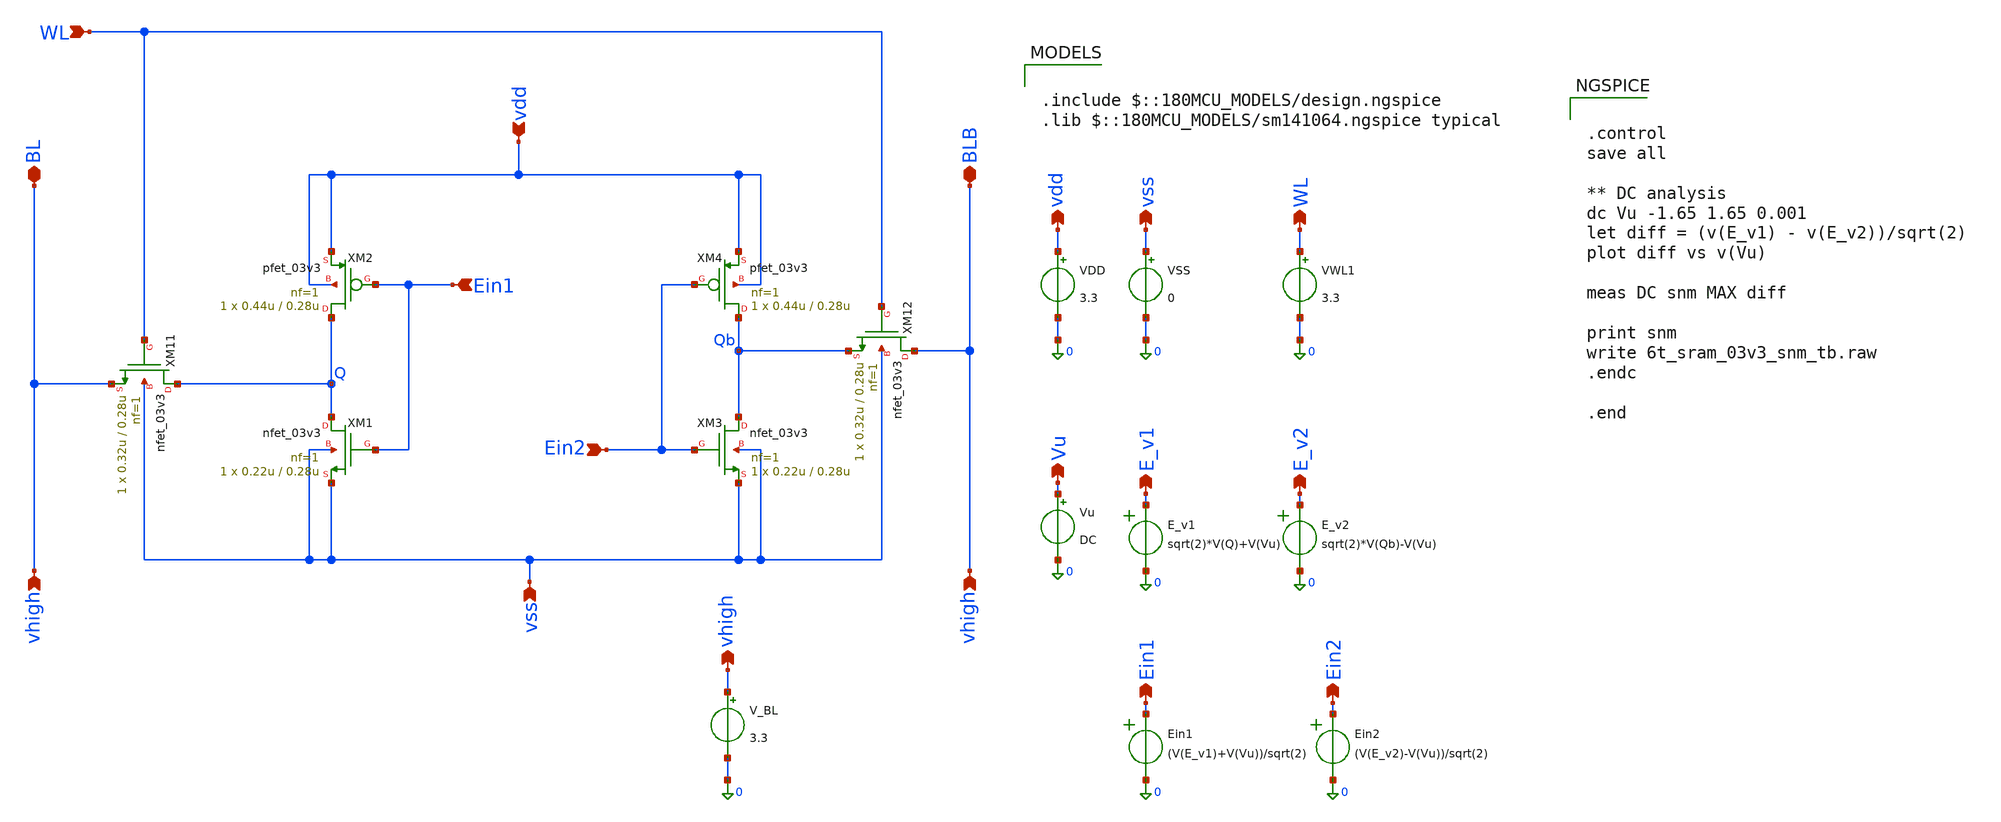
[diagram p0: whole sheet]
** sch_path: analog/tests/6t_sram_03v3_write_seevinck_tb.sch
**.subckt 6t_sram_03v3_write_seevinck_tb vdd vss vdd vss Vu BL WL BLB WL E_v1 E_v2 Ein1 Ein2 Ein1
*+ Ein2 vhigh vhigh vhigh
*.ipin vdd
*.ipin vss
*.opin vdd
*.opin vss
*.opin Vu
*.iopin BL
*.ipin WL
*.iopin BLB
*.opin WL
*.opin E_v1
*.opin E_v2
*.opin Ein1
*.opin Ein2
*.ipin Ein1
*.ipin Ein2
*.opin vhigh
*.ipin vhigh
*.ipin vhigh
XM1 Q Ein1 vss vss nfet_03v3 L=0.28u W=0.22u nf=1 ad='int((nf+1)/2) * W/nf * 0.18u' as='int((nf+2)/2) * W/nf * 0.18u'
+ pd='2*int((nf+1)/2) * (W/nf + 0.18u)' ps='2*int((nf+2)/2) * (W/nf + 0.18u)' nrd='0.18u / W' nrs='0.18u / W'
+ sa=0 sb=0 sd=0 m=1
XM2 Q Ein1 vdd vdd pfet_03v3 L=0.28u W=0.44u nf=1 ad='int((nf+1)/2) * W/nf * 0.18u' as='int((nf+2)/2) * W/nf * 0.18u'
+ pd='2*int((nf+1)/2) * (W/nf + 0.18u)' ps='2*int((nf+2)/2) * (W/nf + 0.18u)' nrd='0.18u / W' nrs='0.18u / W'
+ sa=0 sb=0 sd=0 m=1
XM3 Qb Ein2 vss vss nfet_03v3 L=0.28u W=0.22u nf=1 ad='int((nf+1)/2) * W/nf * 0.18u' as='int((nf+2)/2) * W/nf * 0.18u'
+ pd='2*int((nf+1)/2) * (W/nf + 0.18u)' ps='2*int((nf+2)/2) * (W/nf + 0.18u)' nrd='0.18u / W' nrs='0.18u / W'
+ sa=0 sb=0 sd=0 m=1
XM4 Qb Ein2 vdd vdd pfet_03v3 L=0.28u W=0.44u nf=1 ad='int((nf+1)/2) * W/nf * 0.18u' as='int((nf+2)/2) * W/nf * 0.18u'
+ pd='2*int((nf+1)/2) * (W/nf + 0.18u)' ps='2*int((nf+2)/2) * (W/nf + 0.18u)' nrd='0.18u / W' nrs='0.18u / W'
+ sa=0 sb=0 sd=0 m=1
VDD vdd 0 3.3
VSS vss 0 0
Vu Vu 0 DC
XM11 Q WL BL vss nfet_03v3 L=0.28u W=0.32u nf=1 ad='int((nf+1)/2) * W/nf * 0.18u' as='int((nf+2)/2) * W/nf * 0.18u'
+ pd='2*int((nf+1)/2) * (W/nf + 0.18u)' ps='2*int((nf+2)/2) * (W/nf + 0.18u)' nrd='0.18u / W' nrs='0.18u / W'
+ sa=0 sb=0 sd=0 m=1
XM12 BLB WL Qb vss nfet_03v3 L=0.28u W=0.32u nf=1 ad='int((nf+1)/2) * W/nf * 0.18u' as='int((nf+2)/2) * W/nf * 0.18u'
+ pd='2*int((nf+1)/2) * (W/nf + 0.18u)' ps='2*int((nf+2)/2) * (W/nf + 0.18u)' nrd='0.18u / W' nrs='0.18u / W'
+ sa=0 sb=0 sd=0 m=1
VWL1 WL 0 3.3
E_v1 E_v1 0 VOL=' sqrt(2)*V(Q)+V(Vu) '
E_v2 E_v2 0 VOL=' sqrt(2)*V(Qb)-V(Vu) '
Ein1 Ein1 0 VOL=' (V(E_v1)+V(Vu))/sqrt(2) '
Ein2 Ein2 0 VOL=' (V(E_v2)-V(Vu))/sqrt(2) '
V_BL vhigh 0 3.3
**** begin user architecture code

.include $::180MCU_MODELS/design.ngspice
.lib $::180MCU_MODELS/sm141064.ngspice typical



.control
save all

** DC analysis
dc Vu -1.65 1.65 0.001
let diff = (v(E_v1) - v(E_v2))/sqrt(2)
plot diff vs v(Vu)

meas DC snm MAX diff

print snm
write 6t_sram_03v3_snm_tb.raw
.endc

.end


**** end user architecture code
**.ends
.end
